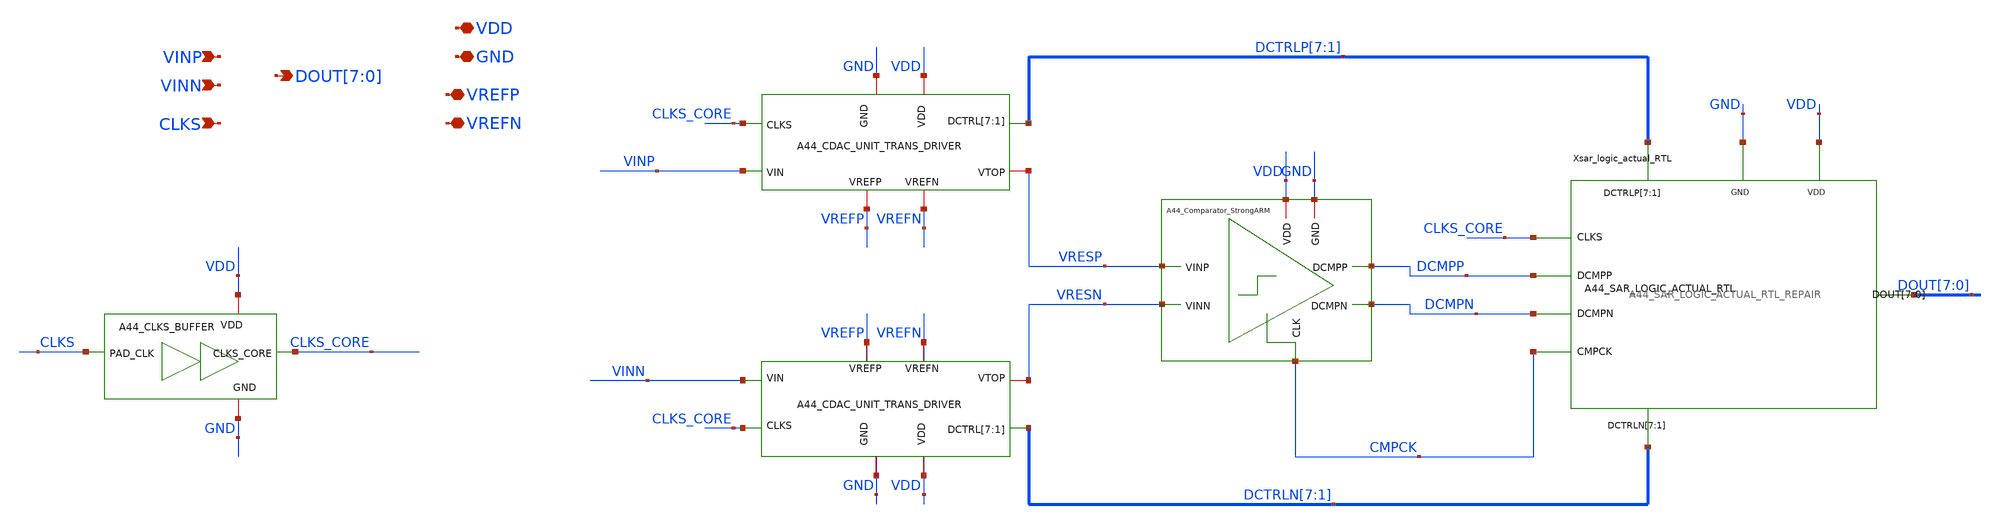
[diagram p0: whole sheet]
** sch_path: verification/a44_w5p29_trans_driver/01_CURRENT_CIRCUIT_FILES/xschem/A44_SAR_ADC_TOP_FIXED.sch
**.subckt A44_SAR_ADC_TOP_FIXED VDD GND VREFP VREFN CLKS VINP VINN
*+ DOUT[7],DOUT[6],DOUT[5],DOUT[4],DOUT[3],DOUT[2],DOUT[1],DOUT[0]
*.iopin VDD
*.iopin GND
*.iopin VREFP
*.iopin VREFN
*.ipin CLKS
*.ipin VINP
*.ipin VINN
*.opin DOUT[7],DOUT[6],DOUT[5],DOUT[4],DOUT[3],DOUT[2],DOUT[1],DOUT[0]
x1 CMPCK DCMPP VRESP DCMPN VRESN VDD GND A44_Comparator_StrongARM
x2 VINP CLKS_CORE VRESP DCTRLP[7] DCTRLP[6] DCTRLP[5] DCTRLP[4] DCTRLP[3] DCTRLP[2] DCTRLP[1] VREFP
+ VDD GND VREFN A44_CDAC_UNIT_TRANS_DRIVER
x3 VINN CLKS_CORE VRESN DCTRLN[7] DCTRLN[6] DCTRLN[5] DCTRLN[4] DCTRLN[3] DCTRLN[2] DCTRLN[1] VREFP
+ VDD GND VREFN A44_CDAC_UNIT_TRANS_DRIVER
Xsar_logic_actual_RTL CLKS_CORE DCMPP DCMPN CMPCK DCTRLP[7] DCTRLP[6] DCTRLP[5] DCTRLP[4] DCTRLP[3]
+ DCTRLP[2] DCTRLP[1] DCTRLN[7] DCTRLN[6] DCTRLN[5] DCTRLN[4] DCTRLN[3] DCTRLN[2] DCTRLN[1] DOUT[7] DOUT[6]
+ DOUT[5] DOUT[4] DOUT[3] DOUT[2] DOUT[1] DOUT[0] VDD GND A44_SAR_LOGIC_ACTUAL_RTL
xclks_buffer VDD GND CLKS_CORE CLKS A44_CLKS_BUFFER
**.ends
.end
